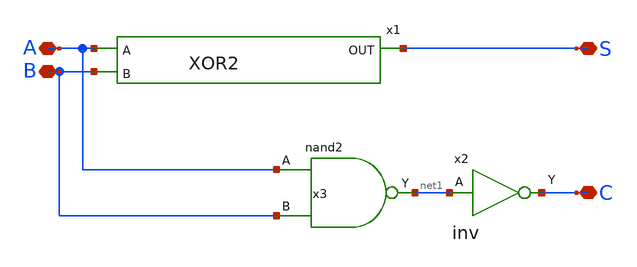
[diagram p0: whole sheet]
** sch_path: design/xschem/ADDER/half_adder.sch
**.subckt half_adder A B S C
*.iopin A
*.iopin B
*.iopin S
*.iopin C
x1 A B S XOR2
x3 A B VSS VDD net1 nand2
x2 net1 VSS VDD C inv
**.ends
.end
